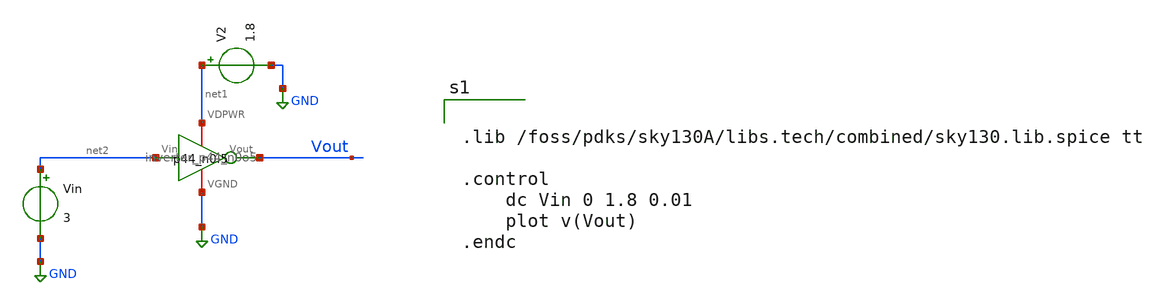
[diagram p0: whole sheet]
** sch_path: xschem/unit_inverter_test.sch
**.subckt unit_inverter_test
Vin net2 GND 3
V2 net1 GND 1.8
x1 net1 Vout net2 GND inverter_p44_n0o5
**** begin user architecture code


.lib /foss/pdks/sky130A/libs.tech/combined/sky130.lib.spice tt

.control
	dc Vin 0 1.8 0.01
	plot v(Vout)
.endc


**** end user architecture code
**.ends

* expanding   symbol:
*+  /foss/designs/analog-circuit-design/sky25a-TIQ_ADC/xschem/INVERTER_SIZES/inverter_p44_n0o5.sym # of pins=4
** sym_path: xschem/INVERTER_SIZES/inverter_p44_n0o5.sym
** sch_path: xschem/INVERTER_SIZES/inverter_p44_n0o5.sch
.subckt inverter_p44_n0o5 VDPWR Vout Vin VGND
*.opin Vout
*.ipin Vin
*.iopin VDPWR
*.iopin VGND
XM1 Vout Vin VGND VGND sky130_fd_pr__nfet_01v8 L=0.15 W=0.5 nf=1 ad='int((nf+1)/2) * W/nf * 0.29' as='int((nf+2)/2) * W/nf * 0.29'
+ pd='2*int((nf+1)/2) * (W/nf + 0.29)' ps='2*int((nf+2)/2) * (W/nf + 0.29)' nrd='0.29 / W' nrs='0.29 / W'
+ sa=0 sb=0 sd=0 mult=1 m=1
XM2 Vout Vin VDPWR VDPWR sky130_fd_pr__pfet_01v8 L=0.15 W=14.67 nf=2 ad='int((nf+1)/2) * W/nf * 0.29'
+ as='int((nf+2)/2) * W/nf * 0.29' pd='2*int((nf+1)/2) * (W/nf + 0.29)' ps='2*int((nf+2)/2) * (W/nf + 0.29)'
+ nrd='0.29 / W' nrs='0.29 / W' sa=0 sb=0 sd=0 mult=1 m=1
XM3 Vout Vin VDPWR VDPWR sky130_fd_pr__pfet_01v8 L=0.15 W=14.67 nf=2 ad='int((nf+1)/2) * W/nf * 0.29'
+ as='int((nf+2)/2) * W/nf * 0.29' pd='2*int((nf+1)/2) * (W/nf + 0.29)' ps='2*int((nf+2)/2) * (W/nf + 0.29)'
+ nrd='0.29 / W' nrs='0.29 / W' sa=0 sb=0 sd=0 mult=1 m=1
XM4 Vout Vin VDPWR VDPWR sky130_fd_pr__pfet_01v8 L=0.15 W=14.67 nf=2 ad='int((nf+1)/2) * W/nf * 0.29'
+ as='int((nf+2)/2) * W/nf * 0.29' pd='2*int((nf+1)/2) * (W/nf + 0.29)' ps='2*int((nf+2)/2) * (W/nf + 0.29)'
+ nrd='0.29 / W' nrs='0.29 / W' sa=0 sb=0 sd=0 mult=1 m=1
.ends

.GLOBAL GND
.end
